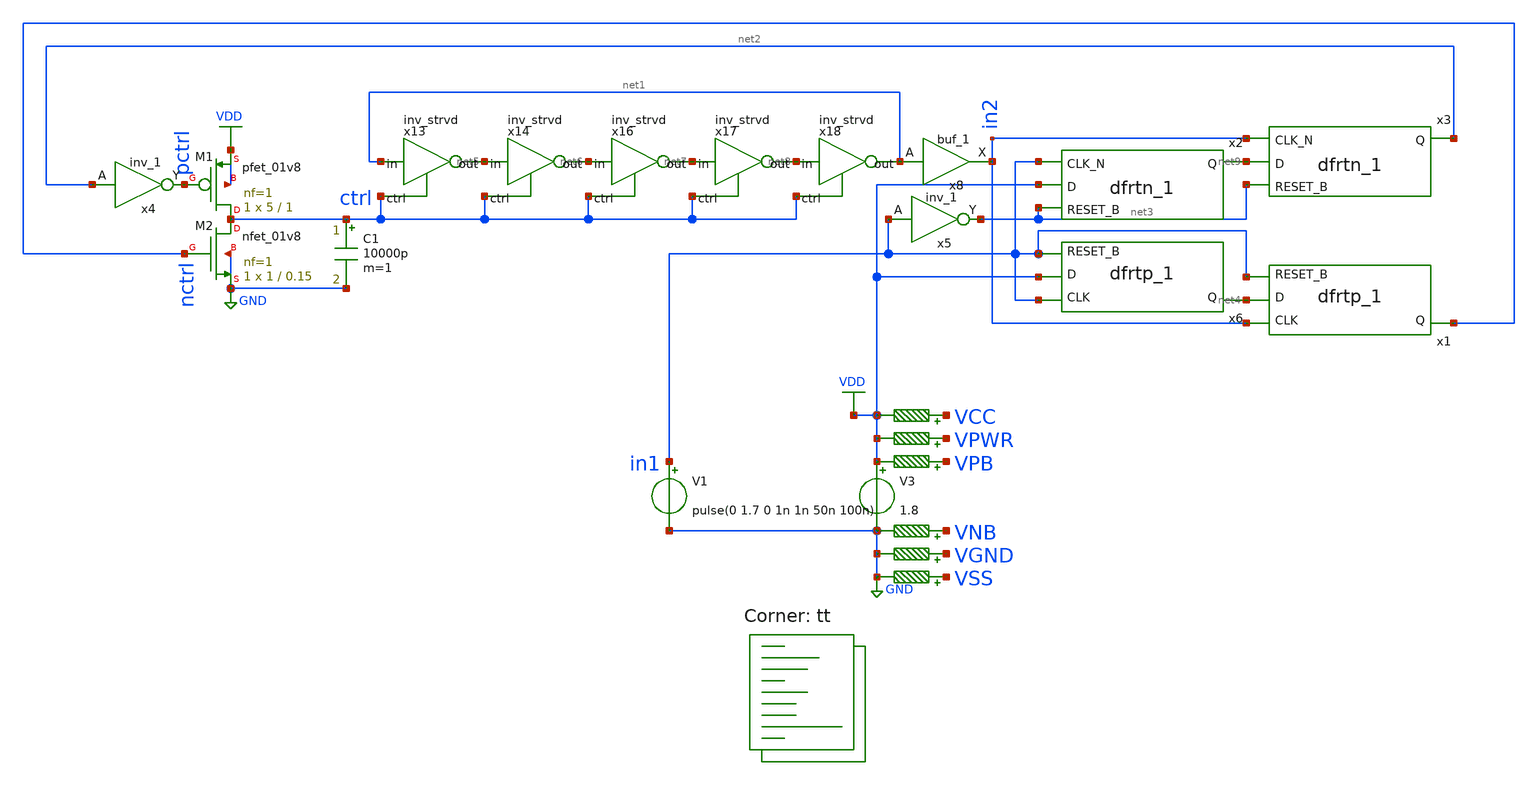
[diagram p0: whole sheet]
** sch_path: archive/freq_det.backup.sch
**.subckt freq_det.backup
V3 VDD GND 1.8
R1 VNB GND 0.01 m=1
R2 VPB VDD 0.01 m=1
R3 VPWR VDD 0.01 m=1
R4 VGND GND 0.01 m=1
R5 VSS GND 0.01 m=1
R6 VCC VDD 0.01 m=1
V1 in1 GND pulse(0 1.7 0 1n 1n 50n 100n)
x6 in1 VDD in1 VGND VNB VPB VPWR net4 sky130_fd_sc_hd__dfrtp_1
x13 net1 net5 ctrl VDD GND inv_strvd
x14 net5 net6 ctrl VDD GND inv_strvd
x16 net6 net7 ctrl VDD GND inv_strvd
x17 net7 net8 ctrl VDD GND inv_strvd
x18 net8 net1 ctrl VDD GND inv_strvd
XM1 ctrl pctrl VDD VDD sky130_fd_pr__pfet_01v8 L=1 W=5 nf=1 ad='int((nf+1)/2) * W/nf * 0.29' as='int((nf+2)/2) * W/nf * 0.29'
+ pd='2*int((nf+1)/2) * (W/nf + 0.29)' ps='2*int((nf+2)/2) * (W/nf + 0.29)' nrd='0.29 / W' nrs='0.29 / W'
+ sa=0 sb=0 sd=0 mult=1 m=1
XM2 ctrl nctrl GND GND sky130_fd_pr__nfet_01v8 L=0.15 W=1 nf=1 ad='int((nf+1)/2) * W/nf * 0.29' as='int((nf+2)/2) * W/nf * 0.29'
+ pd='2*int((nf+1)/2) * (W/nf + 0.29)' ps='2*int((nf+2)/2) * (W/nf + 0.29)' nrd='0.29 / W' nrs='0.29 / W'
+ sa=0 sb=0 sd=0 mult=1 m=1
C1 ctrl GND 10000p m=1
x8 net1 VGND VNB VPB VPWR in2 sky130_fd_sc_hd__buf_1
x1 in2 net4 in1 VGND VNB VPB VPWR nctrl sky130_fd_sc_hd__dfrtp_1
x2 in1 VDD net3 VGND VNB VPB VPWR net9 sky130_fd_sc_hd__dfrtn_1
x3 in2 net9 net3 VGND VNB VPB VPWR net2 sky130_fd_sc_hd__dfrtn_1
x4 net2 VGND VNB VPB VPWR pctrl sky130_fd_sc_hd__inv_1
x5 in1 VGND VNB VPB VPWR net3 sky130_fd_sc_hd__inv_1
**** begin user architecture code
.lib $::SKYWATER_MODELS/sky130.lib.spice tt


.include /usr/local/share/pdk/sky130A/libs.ref/sky130_fd_sc_hd/spice/sky130_fd_sc_hd.spice tt
.control
  save all
  tran .1u 200u
  write top.raw
  quit 0
.endc


**** end user architecture code
**.ends

* expanding   symbol:  tt_um_wulf_8bit_vco/xschem/lib/inv_strvd.sym # of pins=3
** sym_path: archive/tt_um_wulf_8bit_vco/xschem/lib/inv_strvd.sym
** sch_path: archive/tt_um_wulf_8bit_vco/xschem/lib/inv_strvd.sch
.subckt inv_strvd in out ctrl VDD VSS
*.ipin in
*.ipin ctrl
*.opin out
XM2 out in net1 net1 sky130_fd_pr__nfet_01v8 L=1 W=40 nf=1 ad='int((1 + 1)/2) * 40 / 1 * 0.29' as='int((1 + 2)/2) * 40 / 1 * 0.29'
+ pd='2*int((1 + 1)/2) * (40 / 1 + 0.29)' ps='2*int((1 + 2)/2) * (40 / 1 + 0.29)' nrd='0.29 / 40 ' nrs='0.29 / 40 '
+ sa=0 sb=0 sd=0 mult=1 m=1
XM3 net1 ctrl VSS VSS sky130_fd_pr__nfet_01v8 L=0.15 W=1 nf=1 ad='int((1 + 1)/2) * 1 / 1 * 0.29' as='int((1 + 2)/2) * 1 / 1 * 0.29'
+ pd='2*int((1 + 1)/2) * (1 / 1 + 0.29)' ps='2*int((1 + 2)/2) * (1 / 1 + 0.29)' nrd='0.29 / 1 ' nrs='0.29 / 1 '
+ sa=0 sb=0 sd=0 mult=1 m=1
XM1 out in VDD VDD sky130_fd_pr__pfet_01v8 L=4 W=40 nf=1 ad='int((nf+1)/2) * W/nf * 0.29' as='int((nf+2)/2) * W/nf * 0.29'
+ pd='2*int((nf+1)/2) * (W/nf + 0.29)' ps='2*int((nf+2)/2) * (W/nf + 0.29)' nrd='0.29 / W' nrs='0.29 / W'
+ sa=0 sb=0 sd=0 mult=1 m=1
.ends

.GLOBAL GND
.GLOBAL VDD
.end
